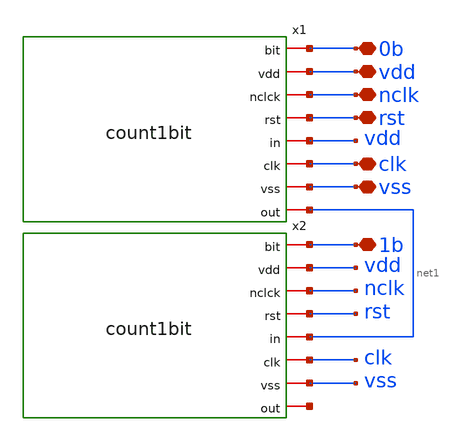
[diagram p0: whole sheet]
** sch_path: design/blocks/count2bits/schematic/count2bits.sch
**.subckt count2bits vdd clk rst 0b nclk vss 1b
*.iopin vdd
*.iopin clk
*.iopin rst
*.iopin 0b
*.iopin nclk
*.iopin vss
*.iopin 1b
x1 0b vdd nclk rst vdd clk vss net1 count1bit
x2 1b vdd nclk rst net1 clk vss net2 count1bit
**.ends
.end
